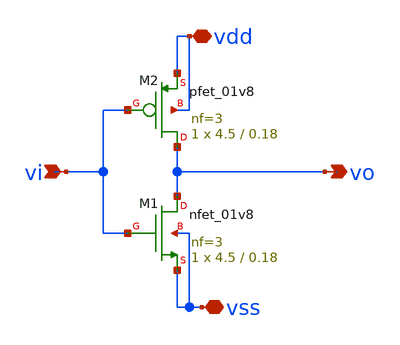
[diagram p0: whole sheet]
** sch_path: Day2_Lab/code/xschem/inverter.sch
**.subckt inverter vi vo vdd vss
*.ipin vi
*.opin vo
*.iopin vdd
*.iopin vss
XM1 vo vi vss vss sky130_fd_pr__nfet_01v8 L=0.18 W=4.5 nf=3 ad='int((nf+1)/2) * W/nf * 0.29' as='int((nf+2)/2) * W/nf * 0.29'
+ pd='2*int((nf+1)/2) * (W/nf + 0.29)' ps='2*int((nf+2)/2) * (W/nf + 0.29)' nrd='0.29 / W' nrs='0.29 / W'
+ sa=0 sb=0 sd=0 mult=1 m=1
XM2 vo vi vdd vdd sky130_fd_pr__pfet_01v8 L=0.18 W=4.5 nf=3 ad='int((nf+1)/2) * W/nf * 0.29' as='int((nf+2)/2) * W/nf * 0.29'
+ pd='2*int((nf+1)/2) * (W/nf + 0.29)' ps='2*int((nf+2)/2) * (W/nf + 0.29)' nrd='0.29 / W' nrs='0.29 / W'
+ sa=0 sb=0 sd=0 mult=1 m=1
**.ends
.end
